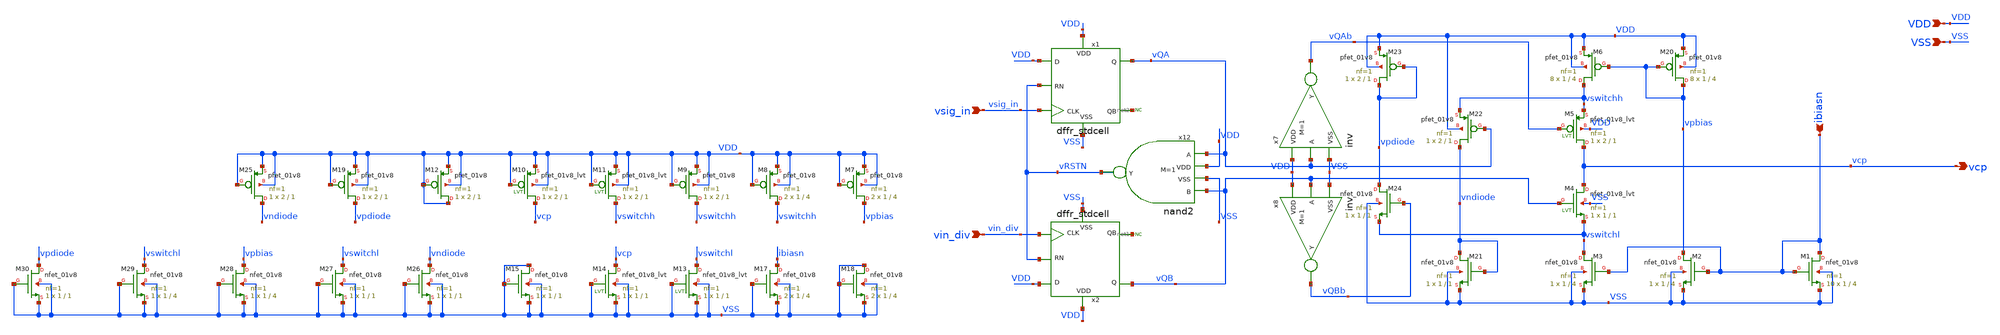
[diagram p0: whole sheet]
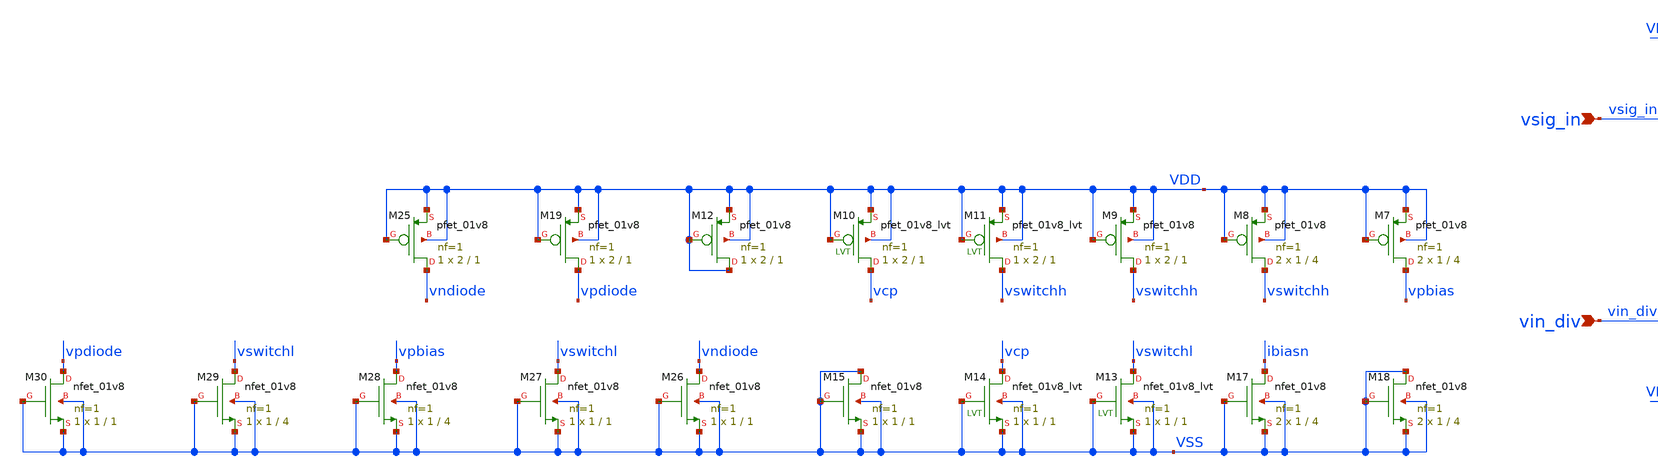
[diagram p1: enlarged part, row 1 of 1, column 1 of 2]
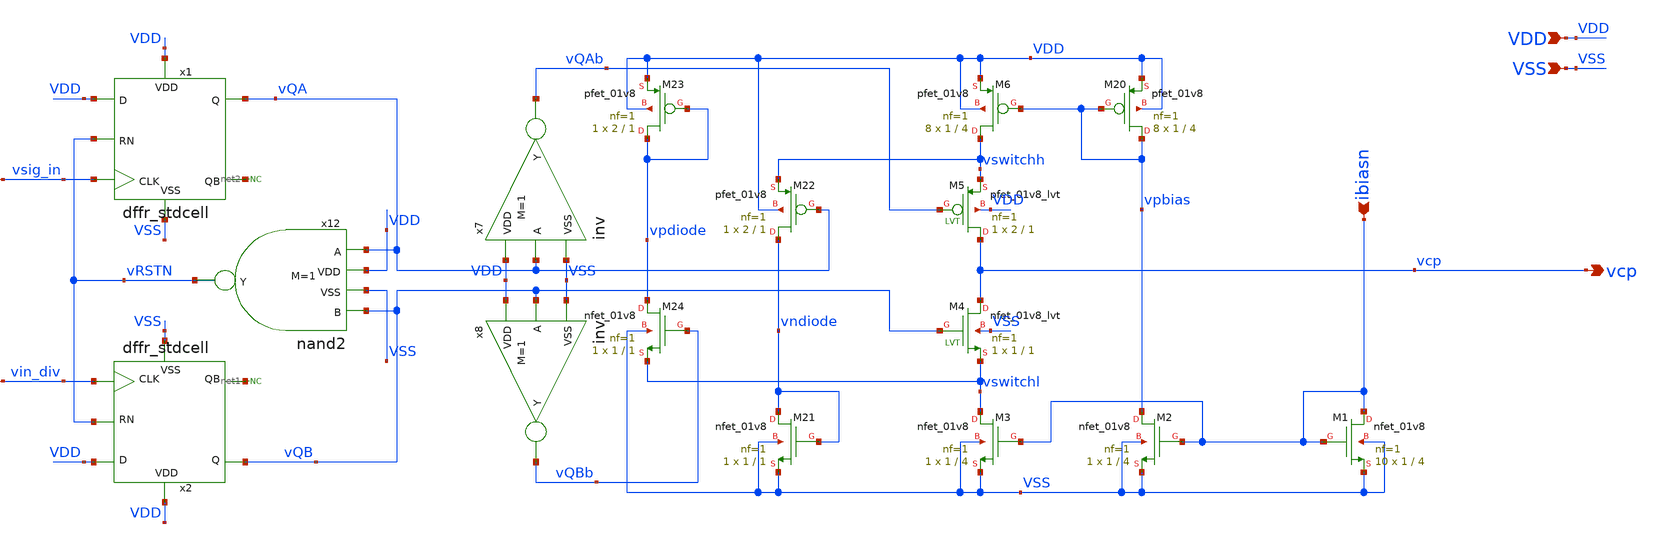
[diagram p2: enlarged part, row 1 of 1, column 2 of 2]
** sch_path: designs/pfd_cp_lpf_lvs.sch
**.subckt pfd_cp_lpf_lvs VDD VSS vin_div vsig_in vcp ibiasn
*.ipin VDD
*.ipin VSS
*.ipin vin_div
*.ipin vsig_in
*.opin vcp
*.ipin ibiasn
XM1 ibiasn ibiasn VSS VSS sky130_fd_pr__nfet_01v8 L=4 W=1 nf=1 ad='int((nf+1)/2) * W/nf * 0.29' as='int((nf+2)/2) * W/nf * 0.29'
+ pd='2*int((nf+1)/2) * (W/nf + 0.29)' ps='2*int((nf+2)/2) * (W/nf + 0.29)' nrd='0.29 / W' nrs='0.29 / W'
+ sa=0 sb=0 sd=0 mult=10 m=10
XM2 vpbias ibiasn VSS VSS sky130_fd_pr__nfet_01v8 L=4 W=1 nf=1 ad='int((nf+1)/2) * W/nf * 0.29' as='int((nf+2)/2) * W/nf * 0.29'
+ pd='2*int((nf+1)/2) * (W/nf + 0.29)' ps='2*int((nf+2)/2) * (W/nf + 0.29)' nrd='0.29 / W' nrs='0.29 / W'
+ sa=0 sb=0 sd=0 mult=1 m=1
XM3 vswitchl ibiasn VSS VSS sky130_fd_pr__nfet_01v8 L=4 W=1 nf=1 ad='int((nf+1)/2) * W/nf * 0.29' as='int((nf+2)/2) * W/nf * 0.29'
+ pd='2*int((nf+1)/2) * (W/nf + 0.29)' ps='2*int((nf+2)/2) * (W/nf + 0.29)' nrd='0.29 / W' nrs='0.29 / W'
+ sa=0 sb=0 sd=0 mult=1 m=1
XM4 vcp vQB vswitchl VSS sky130_fd_pr__nfet_01v8_lvt L=1 W=1 nf=1 ad='int((nf+1)/2) * W/nf * 0.29' as='int((nf+2)/2) * W/nf * 0.29'
+ pd='2*int((nf+1)/2) * (W/nf + 0.29)' ps='2*int((nf+2)/2) * (W/nf + 0.29)' nrd='0.29 / W' nrs='0.29 / W'
+ sa=0 sb=0 sd=0 mult=1 m=1
XM5 vcp vQAb vswitchh VDD sky130_fd_pr__pfet_01v8_lvt L=1 W=2 nf=1 ad='int((nf+1)/2) * W/nf * 0.29' as='int((nf+2)/2) * W/nf * 0.29'
+ pd='2*int((nf+1)/2) * (W/nf + 0.29)' ps='2*int((nf+2)/2) * (W/nf + 0.29)' nrd='0.29 / W' nrs='0.29 / W'
+ sa=0 sb=0 sd=0 mult=1 m=1
XM6 vswitchh vpbias VDD VDD sky130_fd_pr__pfet_01v8 L=4 W=1 nf=1 ad='int((nf+1)/2) * W/nf * 0.29' as='int((nf+2)/2) * W/nf * 0.29'
+ pd='2*int((nf+1)/2) * (W/nf + 0.29)' ps='2*int((nf+2)/2) * (W/nf + 0.29)' nrd='0.29 / W' nrs='0.29 / W'
+ sa=0 sb=0 sd=0 mult=8 m=8
XM20 vpbias vpbias VDD VDD sky130_fd_pr__pfet_01v8 L=4 W=1 nf=1 ad='int((nf+1)/2) * W/nf * 0.29' as='int((nf+2)/2) * W/nf * 0.29'
+ pd='2*int((nf+1)/2) * (W/nf + 0.29)' ps='2*int((nf+2)/2) * (W/nf + 0.29)' nrd='0.29 / W' nrs='0.29 / W'
+ sa=0 sb=0 sd=0 mult=8 m=8
XM21 vndiode vndiode VSS VSS sky130_fd_pr__nfet_01v8 L=1 W=1 nf=1 ad='int((nf+1)/2) * W/nf * 0.29' as='int((nf+2)/2) * W/nf * 0.29'
+ pd='2*int((nf+1)/2) * (W/nf + 0.29)' ps='2*int((nf+2)/2) * (W/nf + 0.29)' nrd='0.29 / W' nrs='0.29 / W'
+ sa=0 sb=0 sd=0 mult=1 m=1
XM22 vndiode vQA vswitchh VDD sky130_fd_pr__pfet_01v8 L=1 W=2 nf=1 ad='int((nf+1)/2) * W/nf * 0.29' as='int((nf+2)/2) * W/nf * 0.29'
+ pd='2*int((nf+1)/2) * (W/nf + 0.29)' ps='2*int((nf+2)/2) * (W/nf + 0.29)' nrd='0.29 / W' nrs='0.29 / W'
+ sa=0 sb=0 sd=0 mult=1 m=1
XM23 vpdiode vpdiode VDD VDD sky130_fd_pr__pfet_01v8 L=1 W=2 nf=1 ad='int((nf+1)/2) * W/nf * 0.29' as='int((nf+2)/2) * W/nf * 0.29'
+ pd='2*int((nf+1)/2) * (W/nf + 0.29)' ps='2*int((nf+2)/2) * (W/nf + 0.29)' nrd='0.29 / W' nrs='0.29 / W'
+ sa=0 sb=0 sd=0 mult=1 m=1
XM24 vpdiode vQBb vswitchl VSS sky130_fd_pr__nfet_01v8 L=1 W=1 nf=1 ad='int((nf+1)/2) * W/nf * 0.29'
+ as='int((nf+2)/2) * W/nf * 0.29' pd='2*int((nf+1)/2) * (W/nf + 0.29)' ps='2*int((nf+2)/2) * (W/nf + 0.29)'
+ nrd='0.29 / W' nrs='0.29 / W' sa=0 sb=0 sd=0 mult=1 m=1
x7 vQA vQAb VDD VSS inv M=1
x8 vQB vQBb VDD VSS inv M=1
x12 vQA vRSTN vQB VDD VSS nand2 M=1
* noconn #net1
* noconn #net2
x1 vRSTN VDD vQA vsig_in net2 VDD VSS dffr_stdcell
x2 vRSTN VDD vQB vin_div net1 VDD VSS dffr_stdcell
XM7 vpbias VDD VDD VDD sky130_fd_pr__pfet_01v8 L=4 W=1 nf=1 ad='int((nf+1)/2) * W/nf * 0.29' as='int((nf+2)/2) * W/nf * 0.29'
+ pd='2*int((nf+1)/2) * (W/nf + 0.29)' ps='2*int((nf+2)/2) * (W/nf + 0.29)' nrd='0.29 / W' nrs='0.29 / W'
+ sa=0 sb=0 sd=0 mult=2 m=2
XM8 vswitchh VDD VDD VDD sky130_fd_pr__pfet_01v8 L=4 W=1 nf=1 ad='int((nf+1)/2) * W/nf * 0.29' as='int((nf+2)/2) * W/nf * 0.29'
+ pd='2*int((nf+1)/2) * (W/nf + 0.29)' ps='2*int((nf+2)/2) * (W/nf + 0.29)' nrd='0.29 / W' nrs='0.29 / W'
+ sa=0 sb=0 sd=0 mult=2 m=2
XM9 vswitchh VDD VDD VDD sky130_fd_pr__pfet_01v8 L=1 W=2 nf=1 ad='int((nf+1)/2) * W/nf * 0.29' as='int((nf+2)/2) * W/nf * 0.29'
+ pd='2*int((nf+1)/2) * (W/nf + 0.29)' ps='2*int((nf+2)/2) * (W/nf + 0.29)' nrd='0.29 / W' nrs='0.29 / W'
+ sa=0 sb=0 sd=0 mult=1 m=1
XM11 vswitchh VDD VDD VDD sky130_fd_pr__pfet_01v8_lvt L=1 W=2 nf=1 ad='int((nf+1)/2) * W/nf * 0.29' as='int((nf+2)/2) * W/nf * 0.29'
+ pd='2*int((nf+1)/2) * (W/nf + 0.29)' ps='2*int((nf+2)/2) * (W/nf + 0.29)' nrd='0.29 / W' nrs='0.29 / W'
+ sa=0 sb=0 sd=0 mult=1 m=1
XM10 vcp VDD VDD VDD sky130_fd_pr__pfet_01v8_lvt L=1 W=2 nf=1 ad='int((nf+1)/2) * W/nf * 0.29' as='int((nf+2)/2) * W/nf * 0.29'
+ pd='2*int((nf+1)/2) * (W/nf + 0.29)' ps='2*int((nf+2)/2) * (W/nf + 0.29)' nrd='0.29 / W' nrs='0.29 / W'
+ sa=0 sb=0 sd=0 mult=1 m=1
XM12 VDD VDD VDD VDD sky130_fd_pr__pfet_01v8 L=1 W=2 nf=1 ad='int((nf+1)/2) * W/nf * 0.29' as='int((nf+2)/2) * W/nf * 0.29'
+ pd='2*int((nf+1)/2) * (W/nf + 0.29)' ps='2*int((nf+2)/2) * (W/nf + 0.29)' nrd='0.29 / W' nrs='0.29 / W'
+ sa=0 sb=0 sd=0 mult=1 m=1
XM13 vswitchl VSS VSS VSS sky130_fd_pr__nfet_01v8_lvt L=1 W=1 nf=1 ad='int((nf+1)/2) * W/nf * 0.29' as='int((nf+2)/2) * W/nf * 0.29'
+ pd='2*int((nf+1)/2) * (W/nf + 0.29)' ps='2*int((nf+2)/2) * (W/nf + 0.29)' nrd='0.29 / W' nrs='0.29 / W'
+ sa=0 sb=0 sd=0 mult=1 m=1
XM14 vcp VSS VSS VSS sky130_fd_pr__nfet_01v8_lvt L=1 W=1 nf=1 ad='int((nf+1)/2) * W/nf * 0.29' as='int((nf+2)/2) * W/nf * 0.29'
+ pd='2*int((nf+1)/2) * (W/nf + 0.29)' ps='2*int((nf+2)/2) * (W/nf + 0.29)' nrd='0.29 / W' nrs='0.29 / W'
+ sa=0 sb=0 sd=0 mult=1 m=1
XM15 VSS VSS VSS VSS sky130_fd_pr__nfet_01v8 L=1 W=1 nf=1 ad='int((nf+1)/2) * W/nf * 0.29' as='int((nf+2)/2) * W/nf * 0.29'
+ pd='2*int((nf+1)/2) * (W/nf + 0.29)' ps='2*int((nf+2)/2) * (W/nf + 0.29)' nrd='0.29 / W' nrs='0.29 / W'
+ sa=0 sb=0 sd=0 mult=1 m=1
XM17 ibiasn VSS VSS VSS sky130_fd_pr__nfet_01v8 L=4 W=1 nf=1 ad='int((nf+1)/2) * W/nf * 0.29' as='int((nf+2)/2) * W/nf * 0.29'
+ pd='2*int((nf+1)/2) * (W/nf + 0.29)' ps='2*int((nf+2)/2) * (W/nf + 0.29)' nrd='0.29 / W' nrs='0.29 / W'
+ sa=0 sb=0 sd=0 mult=2 m=2
XM18 VSS VSS VSS VSS sky130_fd_pr__nfet_01v8 L=4 W=1 nf=1 ad='int((nf+1)/2) * W/nf * 0.29' as='int((nf+2)/2) * W/nf * 0.29'
+ pd='2*int((nf+1)/2) * (W/nf + 0.29)' ps='2*int((nf+2)/2) * (W/nf + 0.29)' nrd='0.29 / W' nrs='0.29 / W'
+ sa=0 sb=0 sd=0 mult=2 m=2
XM19 vpdiode VDD VDD VDD sky130_fd_pr__pfet_01v8 L=1 W=2 nf=1 ad='int((nf+1)/2) * W/nf * 0.29' as='int((nf+2)/2) * W/nf * 0.29'
+ pd='2*int((nf+1)/2) * (W/nf + 0.29)' ps='2*int((nf+2)/2) * (W/nf + 0.29)' nrd='0.29 / W' nrs='0.29 / W'
+ sa=0 sb=0 sd=0 mult=1 m=1
XM25 vndiode VDD VDD VDD sky130_fd_pr__pfet_01v8 L=1 W=2 nf=1 ad='int((nf+1)/2) * W/nf * 0.29' as='int((nf+2)/2) * W/nf * 0.29'
+ pd='2*int((nf+1)/2) * (W/nf + 0.29)' ps='2*int((nf+2)/2) * (W/nf + 0.29)' nrd='0.29 / W' nrs='0.29 / W'
+ sa=0 sb=0 sd=0 mult=1 m=1
XM26 vndiode VSS VSS VSS sky130_fd_pr__nfet_01v8 L=1 W=1 nf=1 ad='int((nf+1)/2) * W/nf * 0.29' as='int((nf+2)/2) * W/nf * 0.29'
+ pd='2*int((nf+1)/2) * (W/nf + 0.29)' ps='2*int((nf+2)/2) * (W/nf + 0.29)' nrd='0.29 / W' nrs='0.29 / W'
+ sa=0 sb=0 sd=0 mult=1 m=1
XM27 vswitchl VSS VSS VSS sky130_fd_pr__nfet_01v8 L=1 W=1 nf=1 ad='int((nf+1)/2) * W/nf * 0.29' as='int((nf+2)/2) * W/nf * 0.29'
+ pd='2*int((nf+1)/2) * (W/nf + 0.29)' ps='2*int((nf+2)/2) * (W/nf + 0.29)' nrd='0.29 / W' nrs='0.29 / W'
+ sa=0 sb=0 sd=0 mult=1 m=1
XM28 vpbias VSS VSS VSS sky130_fd_pr__nfet_01v8 L=4 W=1 nf=1 ad='int((nf+1)/2) * W/nf * 0.29' as='int((nf+2)/2) * W/nf * 0.29'
+ pd='2*int((nf+1)/2) * (W/nf + 0.29)' ps='2*int((nf+2)/2) * (W/nf + 0.29)' nrd='0.29 / W' nrs='0.29 / W'
+ sa=0 sb=0 sd=0 mult=1 m=1
XM29 vswitchl VSS VSS VSS sky130_fd_pr__nfet_01v8 L=4 W=1 nf=1 ad='int((nf+1)/2) * W/nf * 0.29' as='int((nf+2)/2) * W/nf * 0.29'
+ pd='2*int((nf+1)/2) * (W/nf + 0.29)' ps='2*int((nf+2)/2) * (W/nf + 0.29)' nrd='0.29 / W' nrs='0.29 / W'
+ sa=0 sb=0 sd=0 mult=1 m=1
XM30 vpdiode VSS VSS VSS sky130_fd_pr__nfet_01v8 L=1 W=1 nf=1 ad='int((nf+1)/2) * W/nf * 0.29' as='int((nf+2)/2) * W/nf * 0.29'
+ pd='2*int((nf+1)/2) * (W/nf + 0.29)' ps='2*int((nf+2)/2) * (W/nf + 0.29)' nrd='0.29 / W' nrs='0.29 / W'
+ sa=0 sb=0 sd=0 mult=1 m=1
**.ends
.end
